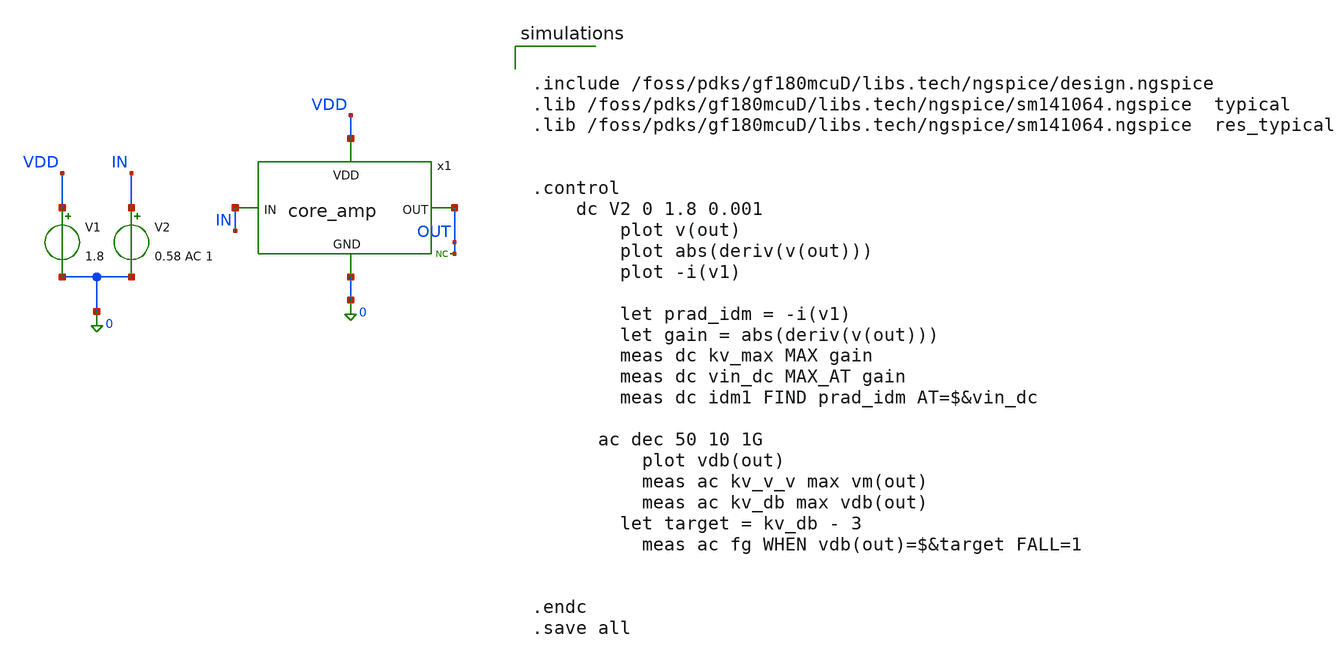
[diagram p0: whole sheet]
** sch_path: core_amp_test.sch
**.subckt core_amp_test
x1 IN OUT VDD 0 core_amp
V1 VDD 0 1.8
* noconn OUT
V2 IN 0 0.58 AC 1
**** begin user architecture code


.include /foss/pdks/gf180mcuD/libs.tech/ngspice/design.ngspice
.lib /foss/pdks/gf180mcuD/libs.tech/ngspice/sm141064.ngspice  typical
.lib /foss/pdks/gf180mcuD/libs.tech/ngspice/sm141064.ngspice  res_typical


.control
	dc V2 0 1.8 0.001
		plot v(out)
		plot abs(deriv(v(out)))
		plot -i(v1)

		let prad_idm = -i(v1)
		let gain = abs(deriv(v(out)))
		meas dc kv_max MAX gain
		meas dc vin_dc MAX_AT gain
		meas dc idm1 FIND prad_idm AT=$&vin_dc

  	ac dec 50 10 1G
  		plot vdb(out)
  		meas ac kv_v_v max vm(out)
  		meas ac kv_db max vdb(out)
		let target = kv_db - 3
  		meas ac fg WHEN vdb(out)=$&target FALL=1


.endc
.save all


name=dc/ac only_toplevel=false
value=
"
.include /foss/pdks/gf180mcuD/libs.tech/ngspice/design.ngspice
.lib /foss/pdks/gf180mcuD/libs.tech/ngspice/sm141064.ngspice  typical
.lib /foss/pdks/gf180mcuD/libs.tech/ngspice/sm141064.ngspice  res_typical


.control
	dc V2 0 1.8 0.001
		plot v(out)
		plot abs(deriv(v(out)))
		plot -i(v1)

		let prad_idm = -i(v1)
		let gain = abs(deriv(v(out)))
		meas dc kv_max MAX gain
		meas dc vin_dc MAX_AT gain
		meas dc idm1 FIND prad_idm AT=$&vin_dc

  	ac dec 50 10 1G
  		plot vdb(out)
  		meas ac kv_v_v max vm(out)
  		meas ac kv_db max vdb(out)
		let target = kv_db - 3
  		meas ac fg WHEN vdb(out)=$&target FALL=1



write plot.raw
.endc
.save all
"
**** end user architecture code
**.ends

* expanding   symbol:  core_amp.sym # of pins=4
** sym_path: core_amp.sym
** sch_path: core_amp.sch
.subckt core_amp IN OUT VDD GND
*.ipin IN
*.opin OUT
*.iopin VDD
*.iopin GND
XM1 OUT IN GND GND nfet_03v3 L=0.28u W=10u nf=1 ad='int((nf+1)/2) * W/nf * 0.18u' as='int((nf+2)/2) * W/nf * 0.18u'
+ pd='2*int((nf+1)/2) * (W/nf + 0.18u)' ps='2*int((nf+2)/2) * (W/nf + 0.18u)' nrd='0.18u / W' nrs='0.18u / W'
+ sa=0 sb=0 sd=0 m=1
XM2 OUT net1 VDD VDD pfet_03v3 L=2.5u W=1u nf=1 ad='int((nf+1)/2) * W/nf * 0.18u' as='int((nf+2)/2) * W/nf * 0.18u'
+ pd='2*int((nf+1)/2) * (W/nf + 0.18u)' ps='2*int((nf+2)/2) * (W/nf + 0.18u)' nrd='0.18u / W' nrs='0.18u / W'
+ sa=0 sb=0 sd=0 m=1
XM3 net1 net1 VDD VDD pfet_03v3 L=2.5u W=1u nf=1 ad='int((nf+1)/2) * W/nf * 0.18u' as='int((nf+2)/2) * W/nf * 0.18u'
+ pd='2*int((nf+1)/2) * (W/nf + 0.18u)' ps='2*int((nf+2)/2) * (W/nf + 0.18u)' nrd='0.18u / W' nrs='0.18u / W'
+ sa=0 sb=0 sd=0 m=1
XRbias GND net1 VDD ppolyf_u r_width=1e-6 r_length=1.05e-6 m=7
.ends

.end
